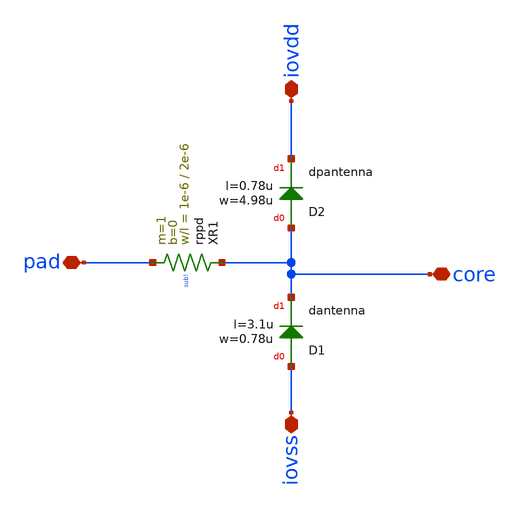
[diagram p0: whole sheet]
** sch_path: ihp-sg13g2/libs.ref/sg13g2_io/xschem/sg13g2_SecondaryProtection.sch
**.subckt sg13g2_SecondaryProtection iovdd iovss core pad
*.iopin iovdd
*.iopin iovss
*.iopin core
*.iopin pad
XR1 pad core sub! rppd w=1e-6 l=2e-6 m=1 b=0
XD1 iovss core dantenna l=3.1u w=0.78u
XD2 core iovdd dpantenna l=0.78u w=4.98u
**.ends
.end
